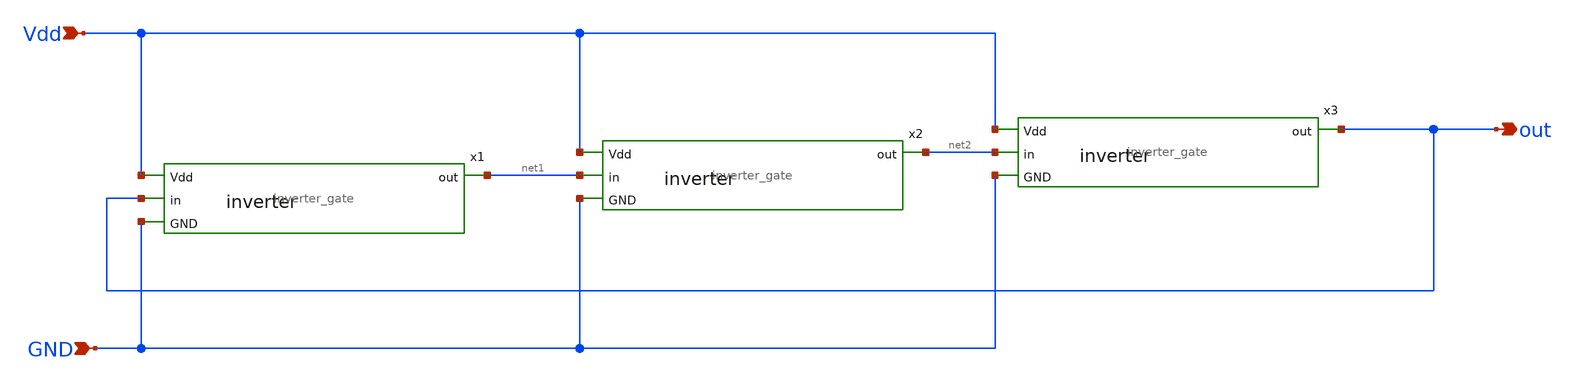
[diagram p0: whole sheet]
** sch_path: RING OSCILLATOR/xschem/ringoscilator.sch
**.subckt ringoscilator out Vdd GND
*.opin out
*.ipin Vdd
*.ipin GND
x1 Vdd out net1 GND inverter_gate
x2 Vdd net1 net2 GND inverter_gate
x3 Vdd net2 out GND inverter_gate
**.ends
.end
